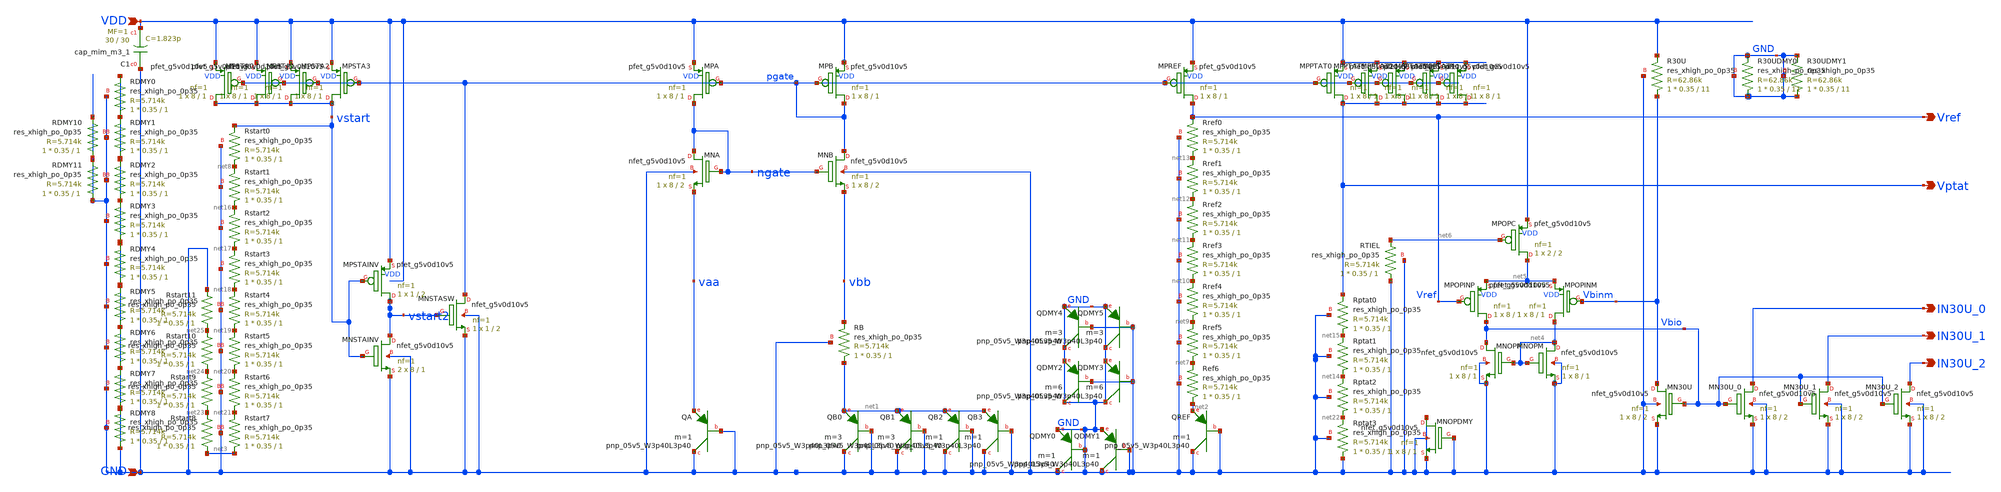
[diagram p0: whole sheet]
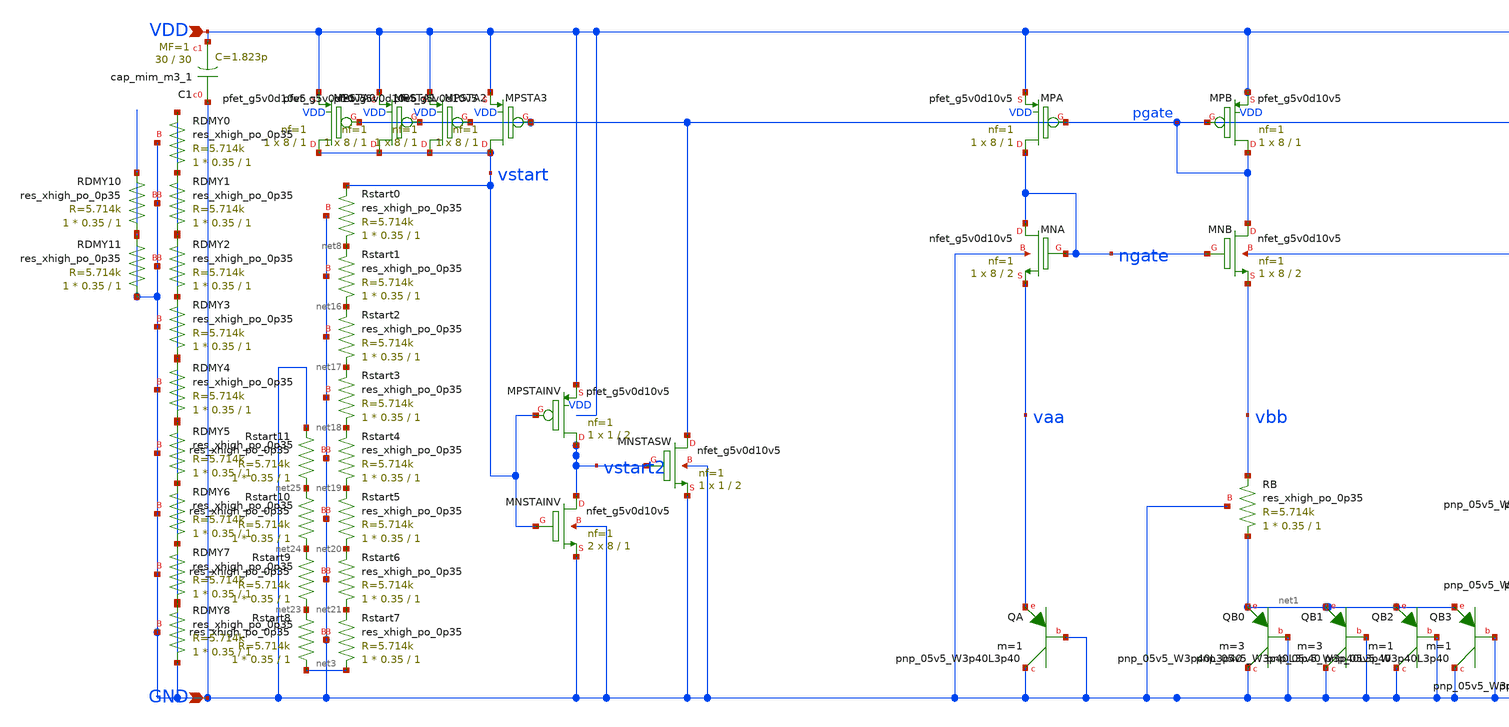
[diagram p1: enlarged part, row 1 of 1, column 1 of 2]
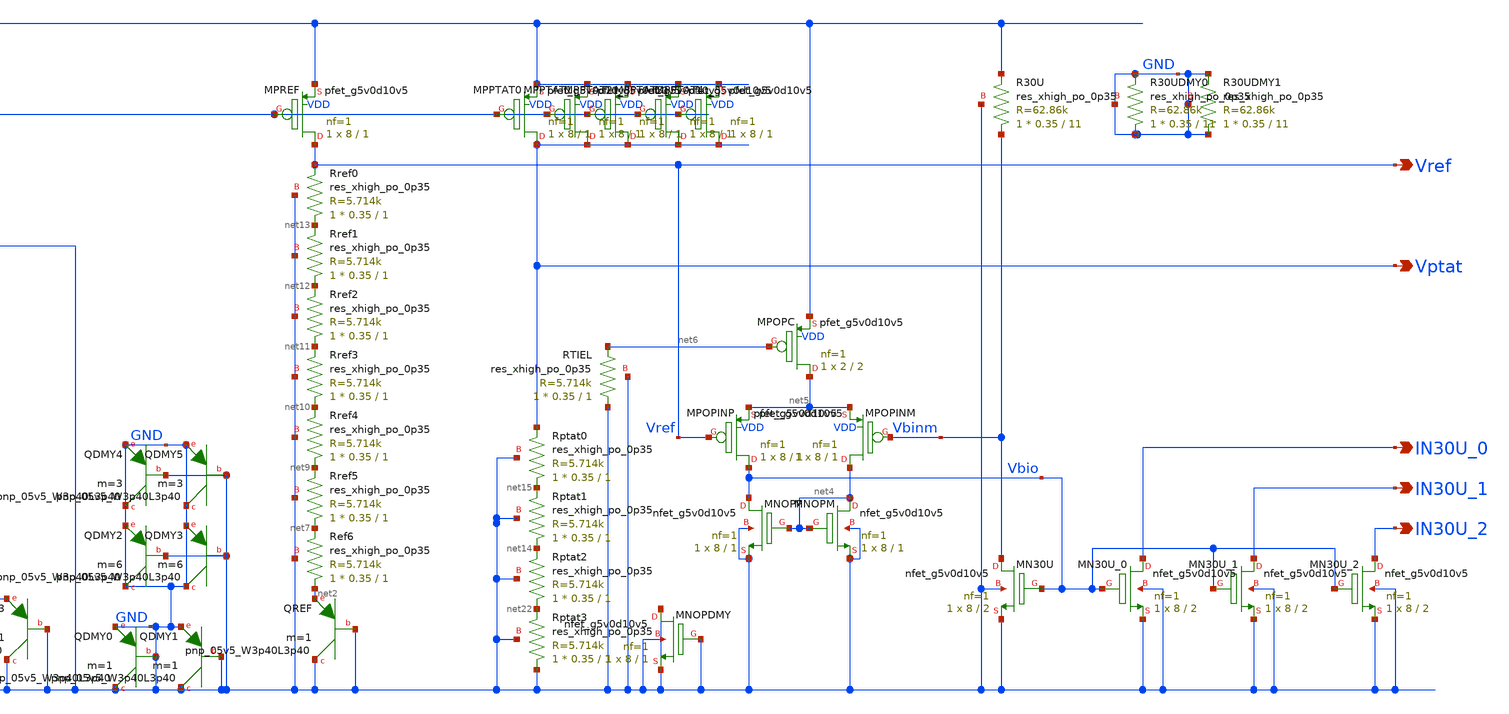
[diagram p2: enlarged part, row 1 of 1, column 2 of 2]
** sch_path: design/schematic/bgr3v3_v1.sch
**.subckt bgr3v3_v1 VDD GND Vref Vptat IN30U_0 IN30U_1 IN30U_2
*.ipin VDD
*.ipin GND
*.opin Vref
*.opin Vptat
*.opin IN30U_0
*.opin IN30U_1
*.opin IN30U_2
XQA GND GND vaa sky130_fd_pr__pnp_05v5_W3p40L3p40 m=1
XQB0 GND GND net1 sky130_fd_pr__pnp_05v5_W3p40L3p40 m=3
XRB net1 vbb GND sky130_fd_pr__res_xhigh_po_0p35 L=1 mult=1 m=1
XRef6 net2 net7 GND sky130_fd_pr__res_xhigh_po_0p35 L=1 mult=1 m=1
XQREF GND GND net2 sky130_fd_pr__pnp_05v5_W3p40L3p40 m=1
XqC1 GND VDD sky130_fd_pr__cap_mim_m3_1 W=30 L=30 MF=1 m=1
XRstart0 net8 vstart GND sky130_fd_pr__res_xhigh_po_0p35 L=1 mult=1 m=1
XRref5 net7 net9 GND sky130_fd_pr__res_xhigh_po_0p35 L=1 mult=1 m=1
XRref4 net9 net10 GND sky130_fd_pr__res_xhigh_po_0p35 L=1 mult=1 m=1
XRref3 net10 net11 GND sky130_fd_pr__res_xhigh_po_0p35 L=1 mult=1 m=1
XRref2 net11 net12 GND sky130_fd_pr__res_xhigh_po_0p35 L=1 mult=1 m=1
XRref1 net12 net13 GND sky130_fd_pr__res_xhigh_po_0p35 L=1 mult=1 m=1
XRref0 net13 Vref GND sky130_fd_pr__res_xhigh_po_0p35 L=1 mult=1 m=1
XRptat1 net14 net15 GND sky130_fd_pr__res_xhigh_po_0p35 L=1 mult=1 m=1
XRptat0 net15 Vptat GND sky130_fd_pr__res_xhigh_po_0p35 L=1 mult=1 m=1
XRstart1 net16 net8 GND sky130_fd_pr__res_xhigh_po_0p35 L=1 mult=1 m=1
XRstart2 net17 net16 GND sky130_fd_pr__res_xhigh_po_0p35 L=1 mult=1 m=1
XRstart3 net18 net17 GND sky130_fd_pr__res_xhigh_po_0p35 L=1 mult=1 m=1
XRstart4 net19 net18 GND sky130_fd_pr__res_xhigh_po_0p35 L=1 mult=1 m=1
XRstart5 net20 net19 GND sky130_fd_pr__res_xhigh_po_0p35 L=1 mult=1 m=1
XRstart6 net21 net20 GND sky130_fd_pr__res_xhigh_po_0p35 L=1 mult=1 m=1
XRstart7 net3 net21 GND sky130_fd_pr__res_xhigh_po_0p35 L=1 mult=1 m=1
XQB1 GND GND net1 sky130_fd_pr__pnp_05v5_W3p40L3p40 m=3
XQB2 GND GND net1 sky130_fd_pr__pnp_05v5_W3p40L3p40 m=1
XQB3 GND GND net1 sky130_fd_pr__pnp_05v5_W3p40L3p40 m=1
XQDMY0 GND GND GND sky130_fd_pr__pnp_05v5_W3p40L3p40 m=1
XQDMY1 GND GND GND sky130_fd_pr__pnp_05v5_W3p40L3p40 m=1
XRptat2 net22 net14 GND sky130_fd_pr__res_xhigh_po_0p35 L=1 mult=1 m=1
XRstart8 net3 net23 GND sky130_fd_pr__res_xhigh_po_0p35 L=1 mult=1 m=1
XRstart9 net23 net24 GND sky130_fd_pr__res_xhigh_po_0p35 L=1 mult=1 m=1
XRstart10 net24 net25 GND sky130_fd_pr__res_xhigh_po_0p35 L=1 mult=1 m=1
XRstart11 net25 GND GND sky130_fd_pr__res_xhigh_po_0p35 L=1 mult=1 m=1
XMPREF Vref pgate VDD VDD sky130_fd_pr__pfet_g5v0d10v5 L=1 W=8 nf=1 ad='int((nf+1)/2) * W/nf * 0.29'
+ as='int((nf+2)/2) * W/nf * 0.29' pd='2*int((nf+1)/2) * (W/nf + 0.29)' ps='2*int((nf+2)/2) * (W/nf + 0.29)'
+ nrd='0.29 / W' nrs='0.29 / W' sa=0 sb=0 sd=0 mult=1 m=1
XMPB pgate pgate VDD VDD sky130_fd_pr__pfet_g5v0d10v5 L=1 W=8 nf=1 ad='int((nf+1)/2) * W/nf * 0.29' as='int((nf+2)/2) * W/nf * 0.29'
+ pd='2*int((nf+1)/2) * (W/nf + 0.29)' ps='2*int((nf+2)/2) * (W/nf + 0.29)' nrd='0.29 / W' nrs='0.29 / W'
+ sa=0 sb=0 sd=0 mult=1 m=1
XMPA ngate pgate VDD VDD sky130_fd_pr__pfet_g5v0d10v5 L=1 W=8 nf=1 ad='int((nf+1)/2) * W/nf * 0.29' as='int((nf+2)/2) * W/nf * 0.29'
+ pd='2*int((nf+1)/2) * (W/nf + 0.29)' ps='2*int((nf+2)/2) * (W/nf + 0.29)' nrd='0.29 / W' nrs='0.29 / W'
+ sa=0 sb=0 sd=0 mult=1 m=1
XMPPTAT0 Vptat pgate VDD VDD sky130_fd_pr__pfet_g5v0d10v5 L=1 W=8 nf=1 ad='int((nf+1)/2) * W/nf * 0.29'
+ as='int((nf+2)/2) * W/nf * 0.29' pd='2*int((nf+1)/2) * (W/nf + 0.29)' ps='2*int((nf+2)/2) * (W/nf + 0.29)'
+ nrd='0.29 / W' nrs='0.29 / W' sa=0 sb=0 sd=0 mult=1 m=1
XMNB pgate ngate vbb GND sky130_fd_pr__nfet_g5v0d10v5 L=2 W=8 nf=1 ad='int((nf+1)/2) * W/nf * 0.29' as='int((nf+2)/2) * W/nf * 0.29'
+ pd='2*int((nf+1)/2) * (W/nf + 0.29)' ps='2*int((nf+2)/2) * (W/nf + 0.29)' nrd='0.29 / W' nrs='0.29 / W'
+ sa=0 sb=0 sd=0 mult=1 m=1
XMNA ngate ngate vaa GND sky130_fd_pr__nfet_g5v0d10v5 L=2 W=8 nf=1 ad='int((nf+1)/2) * W/nf * 0.29' as='int((nf+2)/2) * W/nf * 0.29'
+ pd='2*int((nf+1)/2) * (W/nf + 0.29)' ps='2*int((nf+2)/2) * (W/nf + 0.29)' nrd='0.29 / W' nrs='0.29 / W'
+ sa=0 sb=0 sd=0 mult=1 m=1
XMNSTASW pgate vstart2 GND GND sky130_fd_pr__nfet_g5v0d10v5 L=2 W=1 nf=1 ad='int((nf+1)/2) * W/nf * 0.29'
+ as='int((nf+2)/2) * W/nf * 0.29' pd='2*int((nf+1)/2) * (W/nf + 0.29)' ps='2*int((nf+2)/2) * (W/nf + 0.29)'
+ nrd='0.29 / W' nrs='0.29 / W' sa=0 sb=0 sd=0 mult=1 m=1
XMNSTAINV vstart2 vstart GND GND sky130_fd_pr__nfet_g5v0d10v5 L=1 W=8 nf=1 ad='int((nf+1)/2) * W/nf * 0.29'
+ as='int((nf+2)/2) * W/nf * 0.29' pd='2*int((nf+1)/2) * (W/nf + 0.29)' ps='2*int((nf+2)/2) * (W/nf + 0.29)'
+ nrd='0.29 / W' nrs='0.29 / W' sa=0 sb=0 sd=0 mult=2 m=2
XMPSTAINV vstart2 vstart VDD VDD sky130_fd_pr__pfet_g5v0d10v5 L=2 W=1 nf=1 ad='int((nf+1)/2) * W/nf * 0.29'
+ as='int((nf+2)/2) * W/nf * 0.29' pd='2*int((nf+1)/2) * (W/nf + 0.29)' ps='2*int((nf+2)/2) * (W/nf + 0.29)'
+ nrd='0.29 / W' nrs='0.29 / W' sa=0 sb=0 sd=0 mult=1 m=1
XR30U Vbinm VDD GND sky130_fd_pr__res_xhigh_po_0p35 L=11 mult=1 m=1
XMN30U Vbinm Vbio GND GND sky130_fd_pr__nfet_g5v0d10v5 L=2 W=8 nf=1 ad='int((nf+1)/2) * W/nf * 0.29'
+ as='int((nf+2)/2) * W/nf * 0.29' pd='2*int((nf+1)/2) * (W/nf + 0.29)' ps='2*int((nf+2)/2) * (W/nf + 0.29)'
+ nrd='0.29 / W' nrs='0.29 / W' sa=0 sb=0 sd=0 mult=1 m=1
XMN30U_0 IN30U_0 Vbio GND GND sky130_fd_pr__nfet_g5v0d10v5 L=2 W=8 nf=1 ad='int((nf+1)/2) * W/nf * 0.29'
+ as='int((nf+2)/2) * W/nf * 0.29' pd='2*int((nf+1)/2) * (W/nf + 0.29)' ps='2*int((nf+2)/2) * (W/nf + 0.29)'
+ nrd='0.29 / W' nrs='0.29 / W' sa=0 sb=0 sd=0 mult=1 m=1
XMNOPM net4 net4 GND GND sky130_fd_pr__nfet_g5v0d10v5 L=1 W=8 nf=1 ad='int((nf+1)/2) * W/nf * 0.29' as='int((nf+2)/2) * W/nf * 0.29'
+ pd='2*int((nf+1)/2) * (W/nf + 0.29)' ps='2*int((nf+2)/2) * (W/nf + 0.29)' nrd='0.29 / W' nrs='0.29 / W'
+ sa=0 sb=0 sd=0 mult=1 m=1
XMNOPP Vbio net4 GND GND sky130_fd_pr__nfet_g5v0d10v5 L=1 W=8 nf=1 ad='int((nf+1)/2) * W/nf * 0.29' as='int((nf+2)/2) * W/nf * 0.29'
+ pd='2*int((nf+1)/2) * (W/nf + 0.29)' ps='2*int((nf+2)/2) * (W/nf + 0.29)' nrd='0.29 / W' nrs='0.29 / W'
+ sa=0 sb=0 sd=0 mult=1 m=1
XMPOPINP Vbio Vref net5 VDD sky130_fd_pr__pfet_g5v0d10v5 L=1 W=8 nf=1 ad='int((nf+1)/2) * W/nf * 0.29'
+ as='int((nf+2)/2) * W/nf * 0.29' pd='2*int((nf+1)/2) * (W/nf + 0.29)' ps='2*int((nf+2)/2) * (W/nf + 0.29)'
+ nrd='0.29 / W' nrs='0.29 / W' sa=0 sb=0 sd=0 mult=1 m=1
XMPOPINM net4 Vbinm net5 VDD sky130_fd_pr__pfet_g5v0d10v5 L=1 W=8 nf=1 ad='int((nf+1)/2) * W/nf * 0.29'
+ as='int((nf+2)/2) * W/nf * 0.29' pd='2*int((nf+1)/2) * (W/nf + 0.29)' ps='2*int((nf+2)/2) * (W/nf + 0.29)'
+ nrd='0.29 / W' nrs='0.29 / W' sa=0 sb=0 sd=0 mult=1 m=1
XMPOPC net5 net6 VDD VDD sky130_fd_pr__pfet_g5v0d10v5 L=2 W=2 nf=1 ad='int((nf+1)/2) * W/nf * 0.29' as='int((nf+2)/2) * W/nf * 0.29'
+ pd='2*int((nf+1)/2) * (W/nf + 0.29)' ps='2*int((nf+2)/2) * (W/nf + 0.29)' nrd='0.29 / W' nrs='0.29 / W'
+ sa=0 sb=0 sd=0 mult=1 m=1
XMPSTA0 vstart pgate VDD VDD sky130_fd_pr__pfet_g5v0d10v5 L=1 W=8 nf=1 ad='int((nf+1)/2) * W/nf * 0.29'
+ as='int((nf+2)/2) * W/nf * 0.29' pd='2*int((nf+1)/2) * (W/nf + 0.29)' ps='2*int((nf+2)/2) * (W/nf + 0.29)'
+ nrd='0.29 / W' nrs='0.29 / W' sa=0 sb=0 sd=0 mult=1 m=1
XRptat3 GND net22 GND sky130_fd_pr__res_xhigh_po_0p35 L=1 mult=1 m=1
XMPPTAT1 Vptat pgate VDD VDD sky130_fd_pr__pfet_g5v0d10v5 L=1 W=8 nf=1 ad='int((nf+1)/2) * W/nf * 0.29'
+ as='int((nf+2)/2) * W/nf * 0.29' pd='2*int((nf+1)/2) * (W/nf + 0.29)' ps='2*int((nf+2)/2) * (W/nf + 0.29)'
+ nrd='0.29 / W' nrs='0.29 / W' sa=0 sb=0 sd=0 mult=1 m=1
XMPPTAT2 Vptat pgate VDD VDD sky130_fd_pr__pfet_g5v0d10v5 L=1 W=8 nf=1 ad='int((nf+1)/2) * W/nf * 0.29'
+ as='int((nf+2)/2) * W/nf * 0.29' pd='2*int((nf+1)/2) * (W/nf + 0.29)' ps='2*int((nf+2)/2) * (W/nf + 0.29)'
+ nrd='0.29 / W' nrs='0.29 / W' sa=0 sb=0 sd=0 mult=1 m=1
XMPPTAT3 Vptat pgate VDD VDD sky130_fd_pr__pfet_g5v0d10v5 L=1 W=8 nf=1 ad='int((nf+1)/2) * W/nf * 0.29'
+ as='int((nf+2)/2) * W/nf * 0.29' pd='2*int((nf+1)/2) * (W/nf + 0.29)' ps='2*int((nf+2)/2) * (W/nf + 0.29)'
+ nrd='0.29 / W' nrs='0.29 / W' sa=0 sb=0 sd=0 mult=1 m=1
XMPPTAT4 Vptat pgate VDD VDD sky130_fd_pr__pfet_g5v0d10v5 L=1 W=8 nf=1 ad='int((nf+1)/2) * W/nf * 0.29'
+ as='int((nf+2)/2) * W/nf * 0.29' pd='2*int((nf+1)/2) * (W/nf + 0.29)' ps='2*int((nf+2)/2) * (W/nf + 0.29)'
+ nrd='0.29 / W' nrs='0.29 / W' sa=0 sb=0 sd=0 mult=1 m=1
XMPSTA1 vstart pgate VDD VDD sky130_fd_pr__pfet_g5v0d10v5 L=1 W=8 nf=1 ad='int((nf+1)/2) * W/nf * 0.29'
+ as='int((nf+2)/2) * W/nf * 0.29' pd='2*int((nf+1)/2) * (W/nf + 0.29)' ps='2*int((nf+2)/2) * (W/nf + 0.29)'
+ nrd='0.29 / W' nrs='0.29 / W' sa=0 sb=0 sd=0 mult=1 m=1
XMPSTA2 vstart pgate VDD VDD sky130_fd_pr__pfet_g5v0d10v5 L=1 W=8 nf=1 ad='int((nf+1)/2) * W/nf * 0.29'
+ as='int((nf+2)/2) * W/nf * 0.29' pd='2*int((nf+1)/2) * (W/nf + 0.29)' ps='2*int((nf+2)/2) * (W/nf + 0.29)'
+ nrd='0.29 / W' nrs='0.29 / W' sa=0 sb=0 sd=0 mult=1 m=1
XMPSTA3 vstart pgate VDD VDD sky130_fd_pr__pfet_g5v0d10v5 L=1 W=8 nf=1 ad='int((nf+1)/2) * W/nf * 0.29'
+ as='int((nf+2)/2) * W/nf * 0.29' pd='2*int((nf+1)/2) * (W/nf + 0.29)' ps='2*int((nf+2)/2) * (W/nf + 0.29)'
+ nrd='0.29 / W' nrs='0.29 / W' sa=0 sb=0 sd=0 mult=1 m=1
XMN30U_1 IN30U_1 Vbio GND GND sky130_fd_pr__nfet_g5v0d10v5 L=2 W=8 nf=1 ad='int((nf+1)/2) * W/nf * 0.29'
+ as='int((nf+2)/2) * W/nf * 0.29' pd='2*int((nf+1)/2) * (W/nf + 0.29)' ps='2*int((nf+2)/2) * (W/nf + 0.29)'
+ nrd='0.29 / W' nrs='0.29 / W' sa=0 sb=0 sd=0 mult=1 m=1
XMN30U_2 IN30U_2 Vbio GND GND sky130_fd_pr__nfet_g5v0d10v5 L=2 W=8 nf=1 ad='int((nf+1)/2) * W/nf * 0.29'
+ as='int((nf+2)/2) * W/nf * 0.29' pd='2*int((nf+1)/2) * (W/nf + 0.29)' ps='2*int((nf+2)/2) * (W/nf + 0.29)'
+ nrd='0.29 / W' nrs='0.29 / W' sa=0 sb=0 sd=0 mult=1 m=1
XQDMY2 GND GND GND sky130_fd_pr__pnp_05v5_W3p40L3p40 m=6
XQDMY3 GND GND GND sky130_fd_pr__pnp_05v5_W3p40L3p40 m=6
XQDMY4 GND GND GND sky130_fd_pr__pnp_05v5_W3p40L3p40 m=3
XQDMY5 GND GND GND sky130_fd_pr__pnp_05v5_W3p40L3p40 m=3
XMNOPDMY GND GND GND GND sky130_fd_pr__nfet_g5v0d10v5 L=1 W=8 nf=1 ad='int((nf+1)/2) * W/nf * 0.29' as='int((nf+2)/2) * W/nf * 0.29'
+ pd='2*int((nf+1)/2) * (W/nf + 0.29)' ps='2*int((nf+2)/2) * (W/nf + 0.29)' nrd='0.29 / W' nrs='0.29 / W'
+ sa=0 sb=0 sd=0 mult=1 m=1
XRDMY0 GND GND GND sky130_fd_pr__res_xhigh_po_0p35 L=1 mult=1 m=1
XRDMY1 GND GND GND sky130_fd_pr__res_xhigh_po_0p35 L=1 mult=1 m=1
XRDMY2 GND GND GND sky130_fd_pr__res_xhigh_po_0p35 L=1 mult=1 m=1
XRDMY3 GND GND GND sky130_fd_pr__res_xhigh_po_0p35 L=1 mult=1 m=1
XRDMY4 GND GND GND sky130_fd_pr__res_xhigh_po_0p35 L=1 mult=1 m=1
XRDMY5 GND GND GND sky130_fd_pr__res_xhigh_po_0p35 L=1 mult=1 m=1
XRDMY6 GND GND GND sky130_fd_pr__res_xhigh_po_0p35 L=1 mult=1 m=1
XRDMY7 GND GND GND sky130_fd_pr__res_xhigh_po_0p35 L=1 mult=1 m=1
XRDMY8 GND GND GND sky130_fd_pr__res_xhigh_po_0p35 L=1 mult=1 m=1
XR30UDMY0 GND GND GND sky130_fd_pr__res_xhigh_po_0p35 L=11 mult=1 m=1
XR30UDMY1 GND GND GND sky130_fd_pr__res_xhigh_po_0p35 L=11 mult=1 m=1
XRTIEL GND net6 GND sky130_fd_pr__res_xhigh_po_0p35 L=1 mult=1 m=1
XRDMY10 GND GND GND sky130_fd_pr__res_xhigh_po_0p35 L=1 mult=1 m=1
XRDMY11 GND GND GND sky130_fd_pr__res_xhigh_po_0p35 L=1 mult=1 m=1
**.ends
.end
